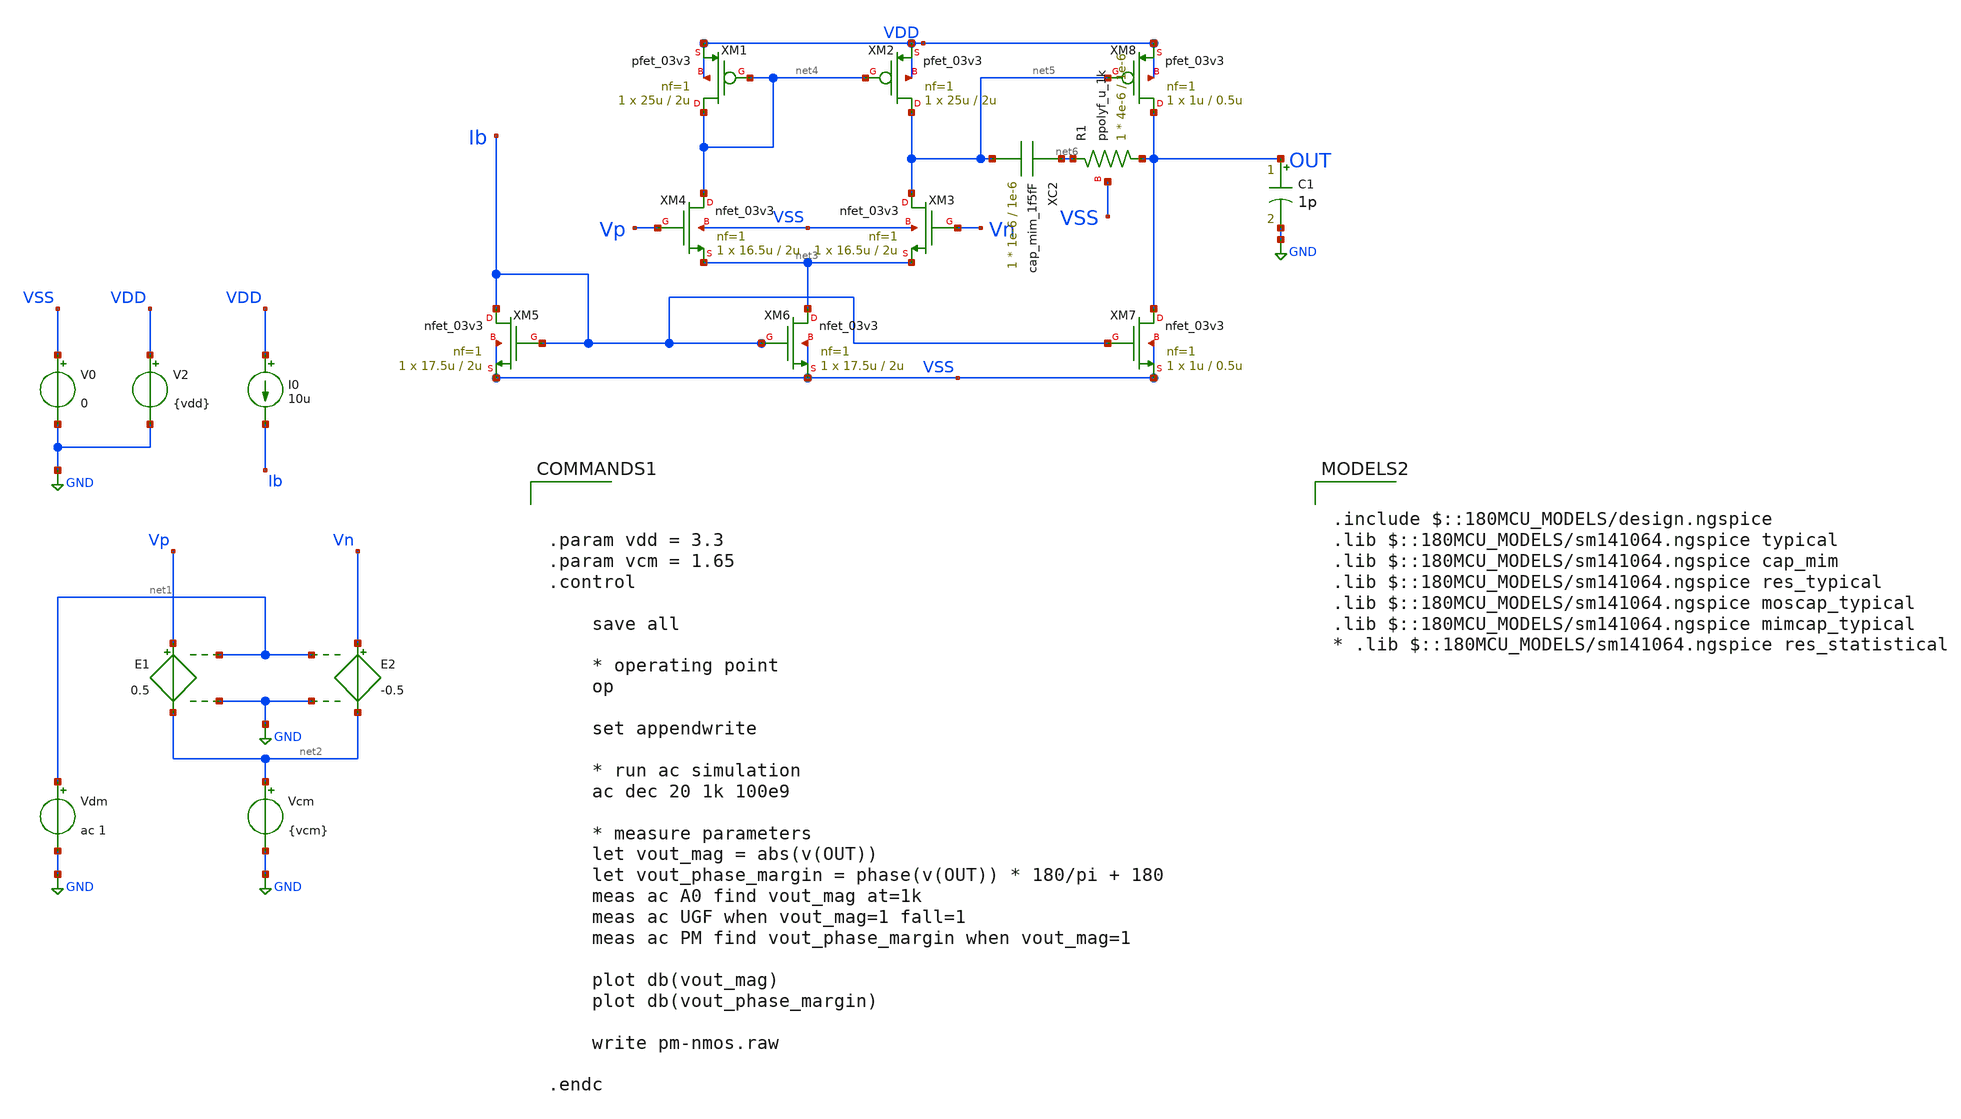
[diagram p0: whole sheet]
** sch_path: designs/libs/tb_ota/tb_nmos-ota/pm-nmos.sch
**.subckt pm-nmos
V0 VSS GND 0
V2 VDD GND {vdd}
E1 Vp net2 net1 GND 0.5
E2 Vn net2 net1 GND -0.5
Vdm net1 GND ac 1
Vcm net2 GND {vcm}
XM1 net4 net4 VDD VDD pfet_03v3 L=2u W=25u nf=1 ad='int((nf+1)/2) * W/nf * 0.18u' as='int((nf+2)/2) * W/nf * 0.18u'
+ pd='2*int((nf+1)/2) * (W/nf + 0.18u)' ps='2*int((nf+2)/2) * (W/nf + 0.18u)' nrd='0.18u / W' nrs='0.18u / W'
+ sa=0 sb=0 sd=0 m=1
XM2 net5 net4 VDD VDD pfet_03v3 L=2u W=25u nf=1 ad='int((nf+1)/2) * W/nf * 0.18u' as='int((nf+2)/2) * W/nf * 0.18u'
+ pd='2*int((nf+1)/2) * (W/nf + 0.18u)' ps='2*int((nf+2)/2) * (W/nf + 0.18u)' nrd='0.18u / W' nrs='0.18u / W'
+ sa=0 sb=0 sd=0 m=1
XM3 net5 Vn net3 VSS nfet_03v3 L=2u W=16.5u nf=1 ad='int((nf+1)/2) * W/nf * 0.18u' as='int((nf+2)/2) * W/nf * 0.18u'
+ pd='2*int((nf+1)/2) * (W/nf + 0.18u)' ps='2*int((nf+2)/2) * (W/nf + 0.18u)' nrd='0.18u / W' nrs='0.18u / W'
+ sa=0 sb=0 sd=0 m=1
XM4 net4 Vp net3 VSS nfet_03v3 L=2u W=16.5u nf=1 ad='int((nf+1)/2) * W/nf * 0.18u' as='int((nf+2)/2) * W/nf * 0.18u'
+ pd='2*int((nf+1)/2) * (W/nf + 0.18u)' ps='2*int((nf+2)/2) * (W/nf + 0.18u)' nrd='0.18u / W' nrs='0.18u / W'
+ sa=0 sb=0 sd=0 m=1
XM6 net3 Ib VSS VSS nfet_03v3 L=2u W=17.5u nf=1 ad='int((nf+1)/2) * W/nf * 0.18u' as='int((nf+2)/2) * W/nf * 0.18u'
+ pd='2*int((nf+1)/2) * (W/nf + 0.18u)' ps='2*int((nf+2)/2) * (W/nf + 0.18u)' nrd='0.18u / W' nrs='0.18u / W'
+ sa=0 sb=0 sd=0 m=1
XM7 OUT Ib VSS VSS nfet_03v3 L=0.5u W=1u nf=1 ad='int((nf+1)/2) * W/nf * 0.18u' as='int((nf+2)/2) * W/nf * 0.18u'
+ pd='2*int((nf+1)/2) * (W/nf + 0.18u)' ps='2*int((nf+2)/2) * (W/nf + 0.18u)' nrd='0.18u / W' nrs='0.18u / W'
+ sa=0 sb=0 sd=0 m=1
XM8 OUT net5 VDD VDD pfet_03v3 L=0.5u W=1u nf=1 ad='int((nf+1)/2) * W/nf * 0.18u' as='int((nf+2)/2) * W/nf * 0.18u'
+ pd='2*int((nf+1)/2) * (W/nf + 0.18u)' ps='2*int((nf+2)/2) * (W/nf + 0.18u)' nrd='0.18u / W' nrs='0.18u / W'
+ sa=0 sb=0 sd=0 m=1
XC2 net6 net5 cap_mim_1f5fF c_width=1e-6 c_length=1e-6 m=1
XR1 OUT net6 VSS ppolyf_u_1k r_width=4e-6 r_length=1e-6 m=1
XM5 Ib Ib VSS VSS nfet_03v3 L=2u W=17.5u nf=1 ad='int((nf+1)/2) * W/nf * 0.18u' as='int((nf+2)/2) * W/nf * 0.18u'
+ pd='2*int((nf+1)/2) * (W/nf + 0.18u)' ps='2*int((nf+2)/2) * (W/nf + 0.18u)' nrd='0.18u / W' nrs='0.18u / W'
+ sa=0 sb=0 sd=0 m=1
I0 VDD Ib 10u
C1 OUT GND 1p m=1
**** begin user architecture code



.param vdd = 3.3
.param vcm = 1.65
.control

    save all

    * operating point
    op

    set appendwrite

    * run ac simulation
    ac dec 20 1k 100e9

    * measure parameters
    let vout_mag = abs(v(OUT))
    let vout_phase_margin = phase(v(OUT)) * 180/pi + 180
    meas ac A0 find vout_mag at=1k
    meas ac UGF when vout_mag=1 fall=1
    meas ac PM find vout_phase_margin when vout_mag=1

	plot db(vout_mag)
	plot db(vout_phase_margin)

    write pm-nmos.raw

.endc



.include $::180MCU_MODELS/design.ngspice
.lib $::180MCU_MODELS/sm141064.ngspice typical
.lib $::180MCU_MODELS/sm141064.ngspice cap_mim
.lib $::180MCU_MODELS/sm141064.ngspice res_typical
.lib $::180MCU_MODELS/sm141064.ngspice moscap_typical
.lib $::180MCU_MODELS/sm141064.ngspice mimcap_typical
* .lib $::180MCU_MODELS/sm141064.ngspice res_statistical

**** end user architecture code
**.ends
.GLOBAL GND
.end
